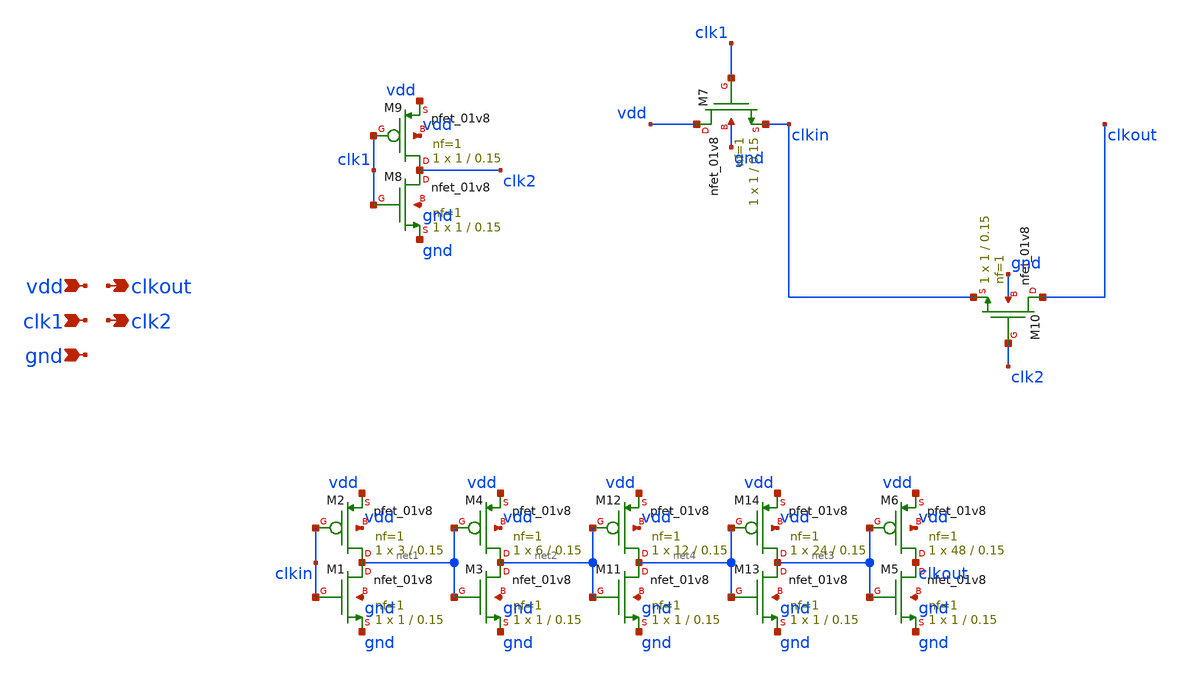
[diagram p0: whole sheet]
** sch_path: week4/xschem/ring-final.sch
**.subckt ring-final vdd gnd clk1 clkout clk2
*.ipin vdd
*.ipin gnd
*.ipin clk1
*.opin clkout
*.opin clk2
XM7 vdd clk1 clkin gnd sky130_fd_pr__nfet_01v8 L=0.15 W=1 nf=1 ad='int((nf+1)/2) * W/nf * 0.29' as='int((nf+2)/2) * W/nf * 0.29'
+ pd='2*int((nf+1)/2) * (W/nf + 0.29)' ps='2*int((nf+2)/2) * (W/nf + 0.29)' nrd='0.29 / W' nrs='0.29 / W'
+ sa=0 sb=0 sd=0 mult=1 m=1
XM8 clk2 clk1 gnd gnd sky130_fd_pr__nfet_01v8 L=0.15 W=1 nf=1 ad='int((nf+1)/2) * W/nf * 0.29' as='int((nf+2)/2) * W/nf * 0.29'
+ pd='2*int((nf+1)/2) * (W/nf + 0.29)' ps='2*int((nf+2)/2) * (W/nf + 0.29)' nrd='0.29 / W' nrs='0.29 / W'
+ sa=0 sb=0 sd=0 mult=1 m=1
XM9 clk2 clk1 vdd vdd sky130_fd_pr__pfet_01v8 L=0.15 W=1 nf=1 ad='int((nf+1)/2) * W/nf * 0.29' as='int((nf+2)/2) * W/nf * 0.29'
+ pd='2*int((nf+1)/2) * (W/nf + 0.29)' ps='2*int((nf+2)/2) * (W/nf + 0.29)' nrd='0.29 / W' nrs='0.29 / W'
+ sa=0 sb=0 sd=0 mult=1 m=1
XM10 clkout clk2 clkin gnd sky130_fd_pr__nfet_01v8 L=0.15 W=1 nf=1 ad='int((nf+1)/2) * W/nf * 0.29' as='int((nf+2)/2) * W/nf * 0.29'
+ pd='2*int((nf+1)/2) * (W/nf + 0.29)' ps='2*int((nf+2)/2) * (W/nf + 0.29)' nrd='0.29 / W' nrs='0.29 / W'
+ sa=0 sb=0 sd=0 mult=1 m=1
XM1 net1 clkin gnd gnd sky130_fd_pr__nfet_01v8 L=0.15 W=1 nf=1 ad='int((nf+1)/2) * W/nf * 0.29' as='int((nf+2)/2) * W/nf * 0.29'
+ pd='2*int((nf+1)/2) * (W/nf + 0.29)' ps='2*int((nf+2)/2) * (W/nf + 0.29)' nrd='0.29 / W' nrs='0.29 / W'
+ sa=0 sb=0 sd=0 mult=1 m=1
XM2 net1 clkin vdd vdd sky130_fd_pr__pfet_01v8 L=0.15 W=3 nf=1 ad='int((nf+1)/2) * W/nf * 0.29' as='int((nf+2)/2) * W/nf * 0.29'
+ pd='2*int((nf+1)/2) * (W/nf + 0.29)' ps='2*int((nf+2)/2) * (W/nf + 0.29)' nrd='0.29 / W' nrs='0.29 / W'
+ sa=0 sb=0 sd=0 mult=1 m=1
XM3 net2 net1 gnd gnd sky130_fd_pr__nfet_01v8 L=0.15 W=1 nf=1 ad='int((nf+1)/2) * W/nf * 0.29' as='int((nf+2)/2) * W/nf * 0.29'
+ pd='2*int((nf+1)/2) * (W/nf + 0.29)' ps='2*int((nf+2)/2) * (W/nf + 0.29)' nrd='0.29 / W' nrs='0.29 / W'
+ sa=0 sb=0 sd=0 mult=1 m=1
XM4 net2 net1 vdd vdd sky130_fd_pr__pfet_01v8 L=0.15 W=6 nf=1 ad='int((nf+1)/2) * W/nf * 0.29' as='int((nf+2)/2) * W/nf * 0.29'
+ pd='2*int((nf+1)/2) * (W/nf + 0.29)' ps='2*int((nf+2)/2) * (W/nf + 0.29)' nrd='0.29 / W' nrs='0.29 / W'
+ sa=0 sb=0 sd=0 mult=1 m=1
XM5 clkout net3 gnd gnd sky130_fd_pr__nfet_01v8 L=0.15 W=1 nf=1 ad='int((nf+1)/2) * W/nf * 0.29' as='int((nf+2)/2) * W/nf * 0.29'
+ pd='2*int((nf+1)/2) * (W/nf + 0.29)' ps='2*int((nf+2)/2) * (W/nf + 0.29)' nrd='0.29 / W' nrs='0.29 / W'
+ sa=0 sb=0 sd=0 mult=1 m=1
XM6 clkout net3 vdd vdd sky130_fd_pr__pfet_01v8 L=0.15 W=48 nf=1 ad='int((nf+1)/2) * W/nf * 0.29' as='int((nf+2)/2) * W/nf * 0.29'
+ pd='2*int((nf+1)/2) * (W/nf + 0.29)' ps='2*int((nf+2)/2) * (W/nf + 0.29)' nrd='0.29 / W' nrs='0.29 / W'
+ sa=0 sb=0 sd=0 mult=1 m=1
XM11 net4 net2 gnd gnd sky130_fd_pr__nfet_01v8 L=0.15 W=1 nf=1 ad='int((nf+1)/2) * W/nf * 0.29' as='int((nf+2)/2) * W/nf * 0.29'
+ pd='2*int((nf+1)/2) * (W/nf + 0.29)' ps='2*int((nf+2)/2) * (W/nf + 0.29)' nrd='0.29 / W' nrs='0.29 / W'
+ sa=0 sb=0 sd=0 mult=1 m=1
XM12 net4 net2 vdd vdd sky130_fd_pr__pfet_01v8 L=0.15 W=12 nf=1 ad='int((nf+1)/2) * W/nf * 0.29' as='int((nf+2)/2) * W/nf * 0.29'
+ pd='2*int((nf+1)/2) * (W/nf + 0.29)' ps='2*int((nf+2)/2) * (W/nf + 0.29)' nrd='0.29 / W' nrs='0.29 / W'
+ sa=0 sb=0 sd=0 mult=1 m=1
XM13 net3 net4 gnd gnd sky130_fd_pr__nfet_01v8 L=0.15 W=1 nf=1 ad='int((nf+1)/2) * W/nf * 0.29' as='int((nf+2)/2) * W/nf * 0.29'
+ pd='2*int((nf+1)/2) * (W/nf + 0.29)' ps='2*int((nf+2)/2) * (W/nf + 0.29)' nrd='0.29 / W' nrs='0.29 / W'
+ sa=0 sb=0 sd=0 mult=1 m=1
XM14 net3 net4 vdd vdd sky130_fd_pr__pfet_01v8 L=0.15 W=24 nf=1 ad='int((nf+1)/2) * W/nf * 0.29' as='int((nf+2)/2) * W/nf * 0.29'
+ pd='2*int((nf+1)/2) * (W/nf + 0.29)' ps='2*int((nf+2)/2) * (W/nf + 0.29)' nrd='0.29 / W' nrs='0.29 / W'
+ sa=0 sb=0 sd=0 mult=1 m=1
**.ends
.end
